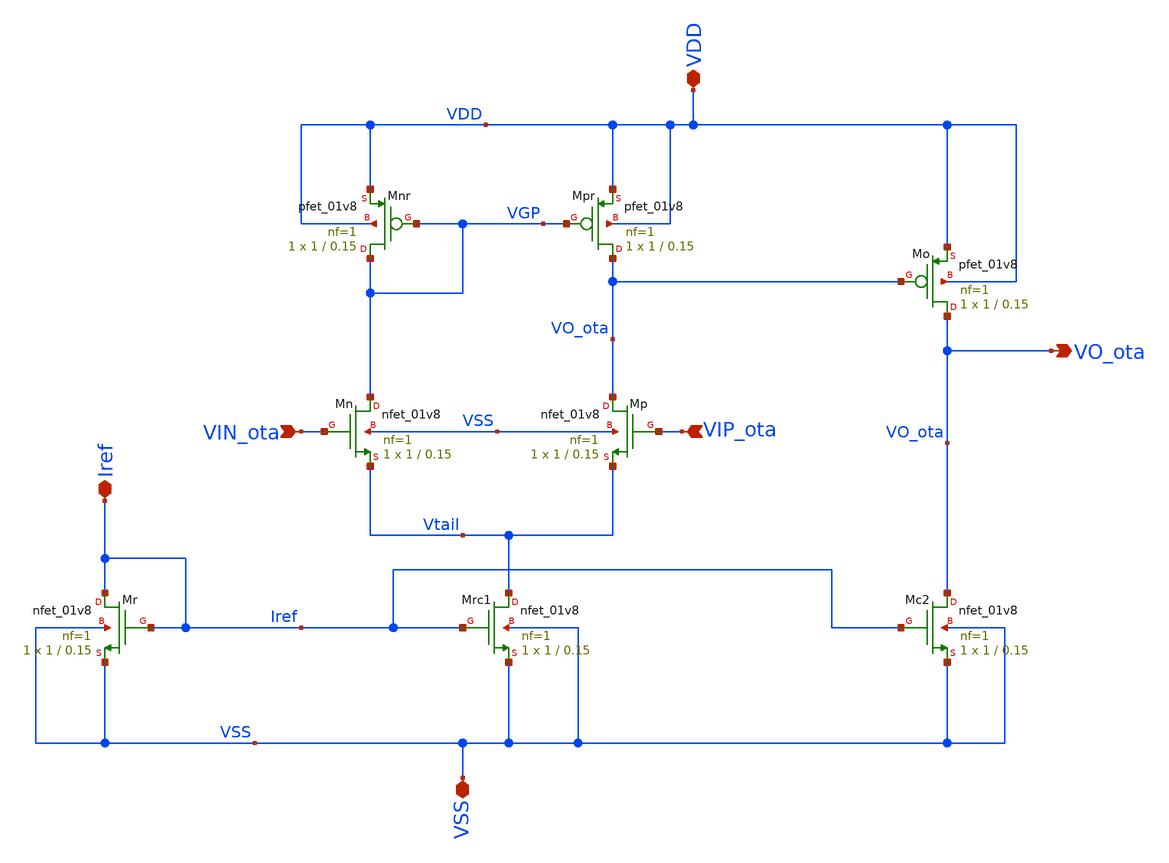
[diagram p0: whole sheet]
** sch_path: xschem/OTA.sch
**.subckt OTA VIN_ota VO_ota Iref VSS VDD VIP_ota
*.ipin VIN_ota
*.opin VO_ota
*.iopin Iref
*.iopin VSS
*.iopin VDD
*.ipin VIP_ota
XMr Iref Iref VSS VSS sky130_fd_pr__nfet_01v8 L=0.15 W=1 nf=1 ad='int((1 + 1)/2) * 1 / 1 * 0.29' as='int((1 + 2)/2) * 1 / 1 * 0.29'
+ pd='2*int((1 + 1)/2) * (1 / 1 + 0.29)' ps='2*int((1 + 2)/2) * (1 / 1 + 0.29)' nrd='0.29 / 1 ' nrs='0.29 / 1 '
+ sa=0 sb=0 sd=0 mult=1 m=1
XMo VO_ota VO_ota VDD VDD sky130_fd_pr__pfet_01v8 L=0.15 W=1 nf=1 ad='int((1 + 1)/2) * 1 / 1 * 0.29'
+ as='int((1 + 2)/2) * 1 / 1 * 0.29' pd='2*int((1 + 1)/2) * (1 / 1 + 0.29)' ps='2*int((1 + 2)/2) * (1 / 1 + 0.29)'
+ nrd='0.29 / 1 ' nrs='0.29 / 1 ' sa=0 sb=0 sd=0 mult=1 m=1
XMrc1 Vtail Iref VSS VSS sky130_fd_pr__nfet_01v8 L=0.15 W=1 nf=1 ad='int((1 + 1)/2) * 1 / 1 * 0.29' as='int((1 + 2)/2) * 1 / 1 * 0.29'
+ pd='2*int((1 + 1)/2) * (1 / 1 + 0.29)' ps='2*int((1 + 2)/2) * (1 / 1 + 0.29)' nrd='0.29 / 1 ' nrs='0.29 / 1 '
+ sa=0 sb=0 sd=0 mult=1 m=1
XMc2 VO_ota Iref VSS VSS sky130_fd_pr__nfet_01v8 L=0.15 W=1 nf=1 ad='int((1 + 1)/2) * 1 / 1 * 0.29' as='int((1 + 2)/2) * 1 / 1 * 0.29'
+ pd='2*int((1 + 1)/2) * (1 / 1 + 0.29)' ps='2*int((1 + 2)/2) * (1 / 1 + 0.29)' nrd='0.29 / 1 ' nrs='0.29 / 1 '
+ sa=0 sb=0 sd=0 mult=1 m=1
XMn VGP VIN_ota Vtail VSS sky130_fd_pr__nfet_01v8 L=0.15 W=1 nf=1 ad='int((1 + 1)/2) * 1 / 1 * 0.29'
+ as='int((1 + 2)/2) * 1 / 1 * 0.29' pd='2*int((1 + 1)/2) * (1 / 1 + 0.29)' ps='2*int((1 + 2)/2) * (1 / 1 + 0.29)'
+ nrd='0.29 / 1 ' nrs='0.29 / 1 ' sa=0 sb=0 sd=0 mult=1 m=1
XMp VO_ota VIP_ota Vtail VSS sky130_fd_pr__nfet_01v8 L=0.15 W=1 nf=1 ad='int((1 + 1)/2) * 1 / 1 * 0.29'
+ as='int((1 + 2)/2) * 1 / 1 * 0.29' pd='2*int((1 + 1)/2) * (1 / 1 + 0.29)' ps='2*int((1 + 2)/2) * (1 / 1 + 0.29)'
+ nrd='0.29 / 1 ' nrs='0.29 / 1 ' sa=0 sb=0 sd=0 mult=1 m=1
XMpr VO_ota VGP VDD VDD sky130_fd_pr__pfet_01v8 L=0.15 W=1 nf=1 ad='int((1 + 1)/2) * 1 / 1 * 0.29' as='int((1 + 2)/2) * 1 / 1 * 0.29'
+ pd='2*int((1 + 1)/2) * (1 / 1 + 0.29)' ps='2*int((1 + 2)/2) * (1 / 1 + 0.29)' nrd='0.29 / 1 ' nrs='0.29 / 1 '
+ sa=0 sb=0 sd=0 mult=1 m=1
XMnr VGP VGP VDD VDD sky130_fd_pr__pfet_01v8 L=0.15 W=1 nf=1 ad='int((1 + 1)/2) * 1 / 1 * 0.29' as='int((1 + 2)/2) * 1 / 1 * 0.29'
+ pd='2*int((1 + 1)/2) * (1 / 1 + 0.29)' ps='2*int((1 + 2)/2) * (1 / 1 + 0.29)' nrd='0.29 / 1 ' nrs='0.29 / 1 '
+ sa=0 sb=0 sd=0 mult=1 m=1
**.ends
.end
